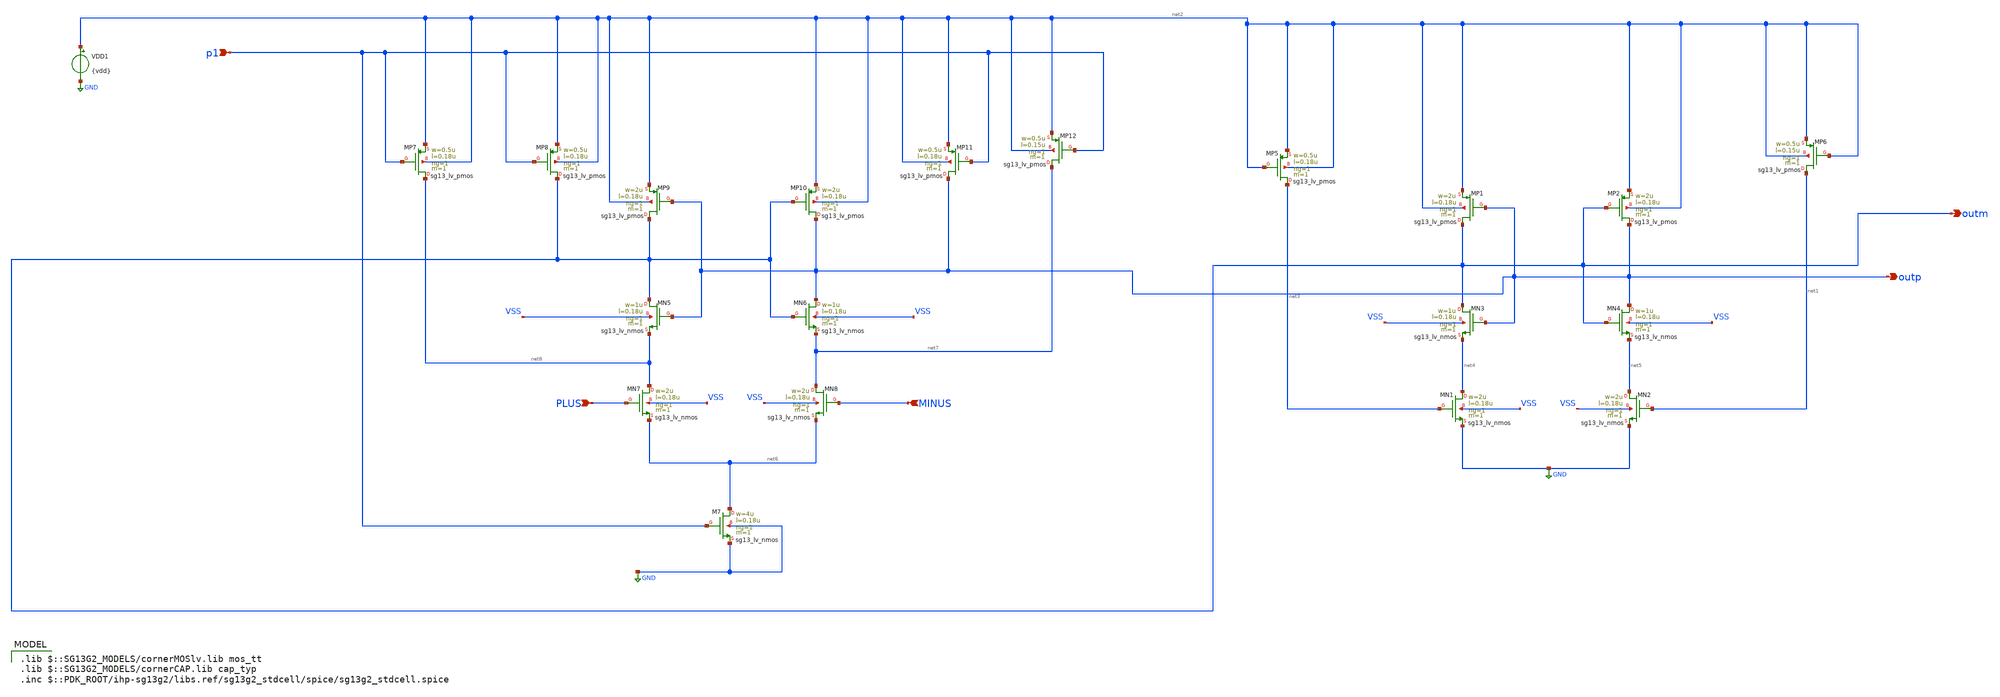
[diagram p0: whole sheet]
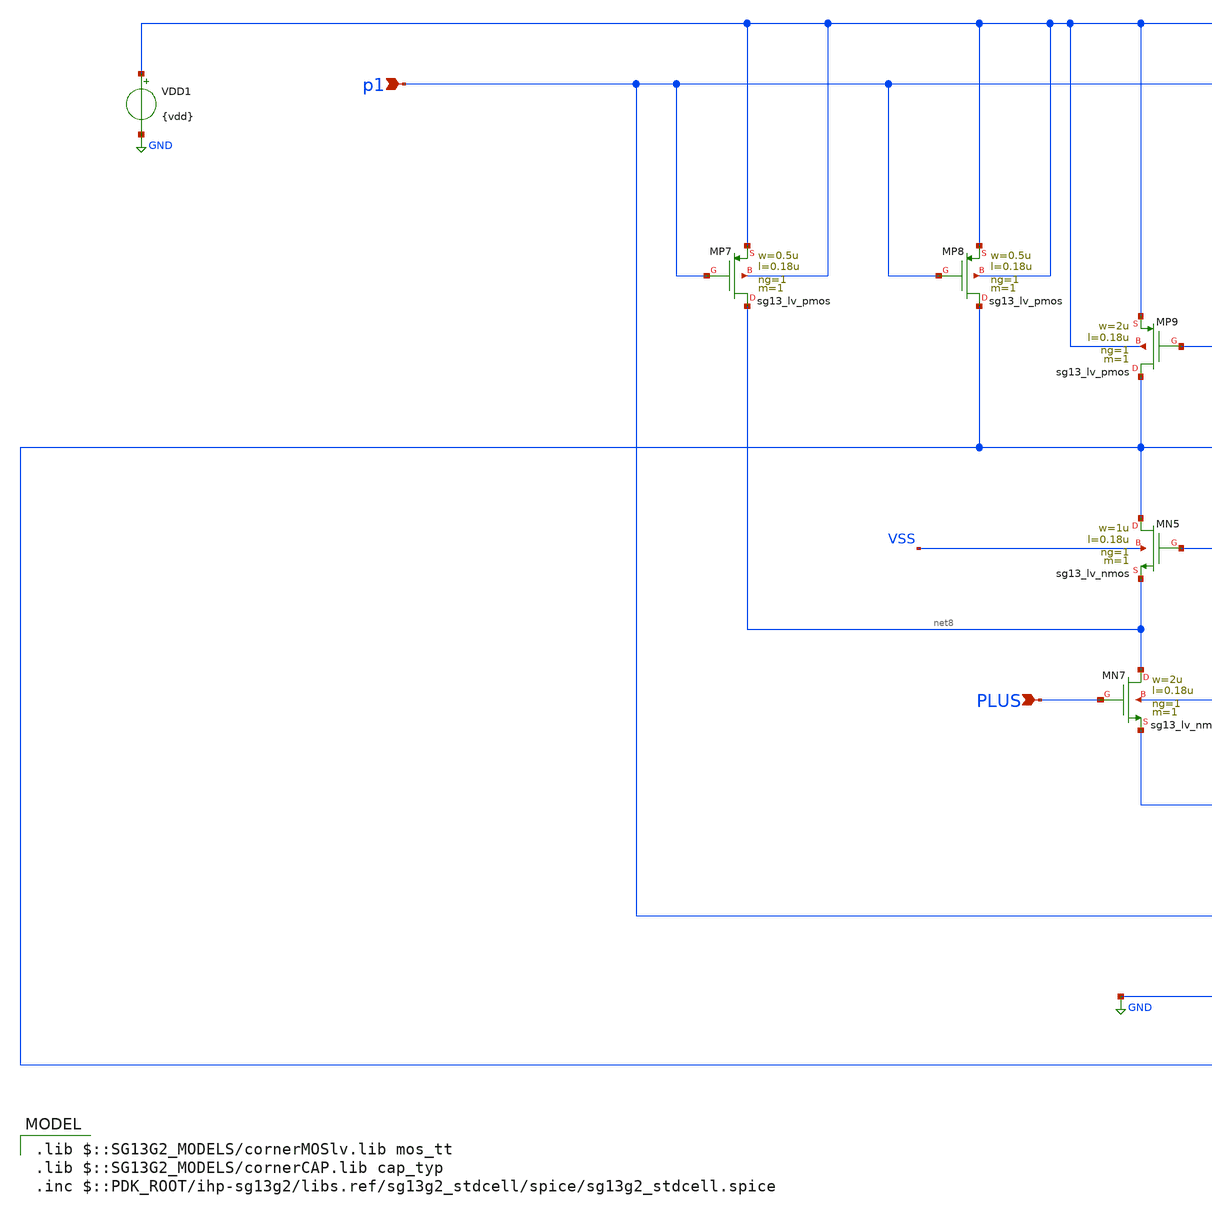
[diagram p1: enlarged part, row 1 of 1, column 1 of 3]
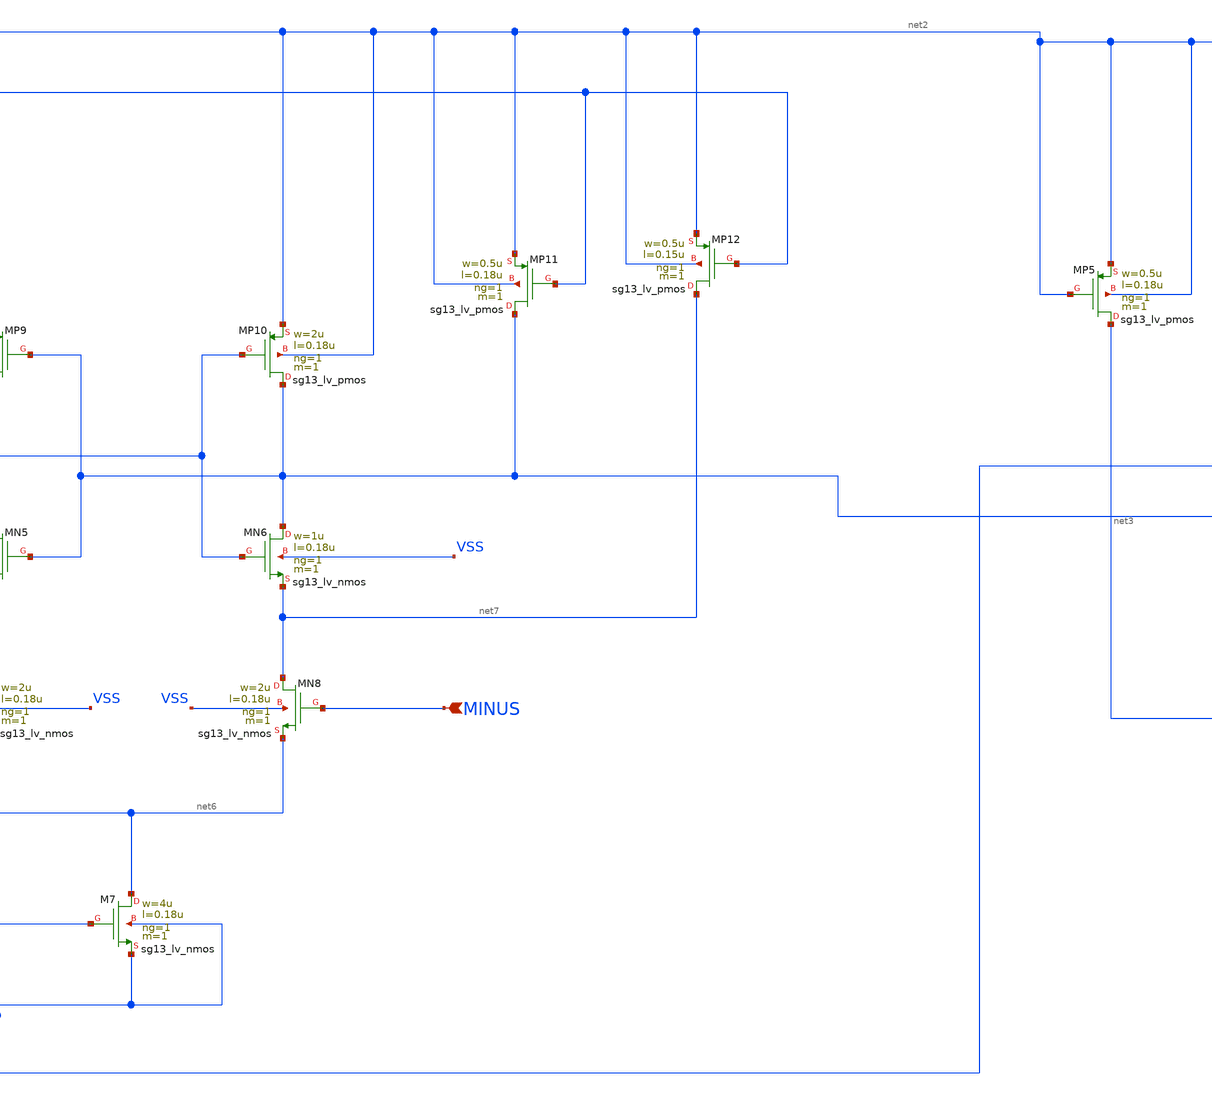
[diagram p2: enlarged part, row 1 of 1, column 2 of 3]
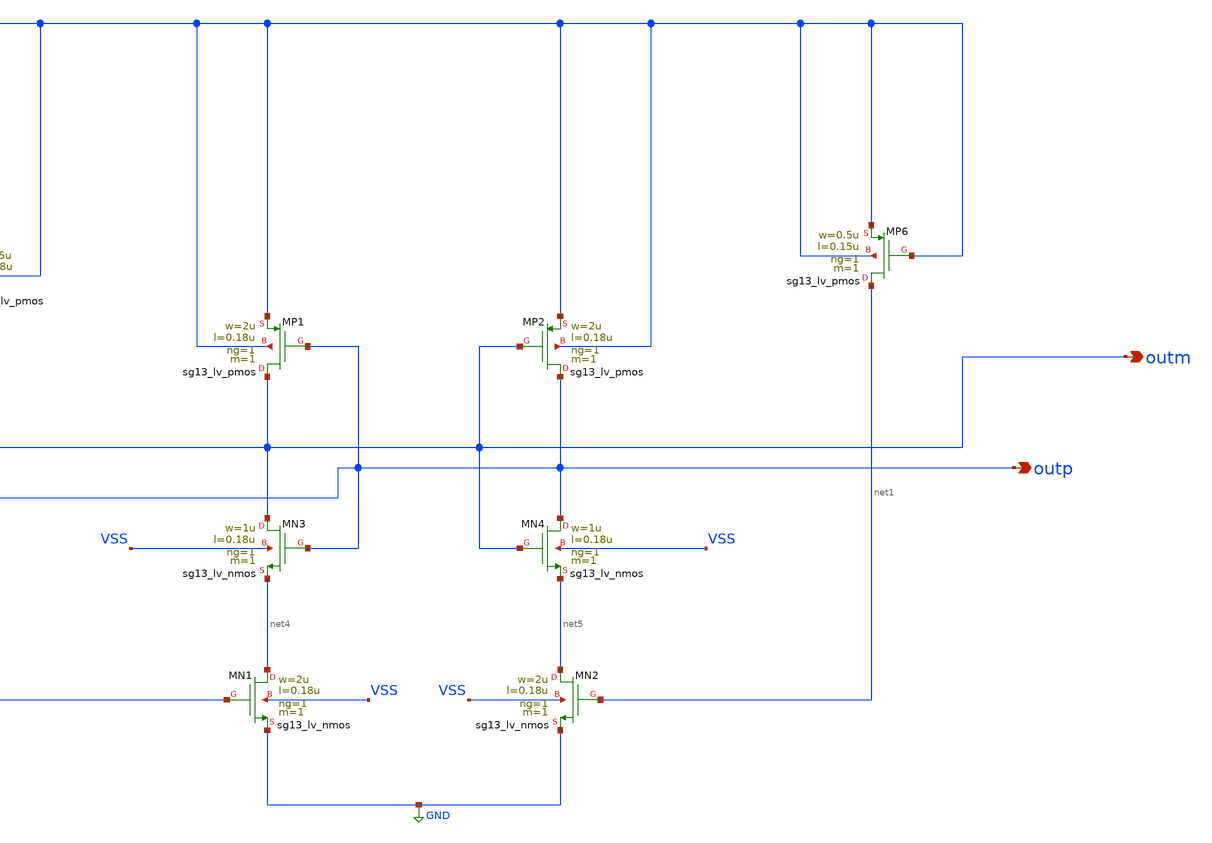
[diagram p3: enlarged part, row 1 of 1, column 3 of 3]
** sch_path: CEMS_G2/DSM/Schematics/RealCircuits/Comp-Latch.sch
**.subckt Comp-Latch outp PLUS MINUS p1 outm
*.opin outp
*.ipin PLUS
*.ipin MINUS
*.ipin p1
*.opin outm
XMN3 outm outp net4 VSS sg13_lv_nmos w=1u l=0.18u ng=1 m=1 mm_ok=1
XMP5 net3 net2 net2 net2 sg13_lv_pmos w=0.5u l=0.18u ng=1 m=1 mm_ok=1
XMP1 outm outp net2 net2 sg13_lv_pmos w=2u l=0.18u ng=1 m=1 mm_ok=1
XMP2 outp outm net2 net2 sg13_lv_pmos w=2u l=0.18u ng=1 m=1 mm_ok=1
XMP6 net1 net2 net2 net2 sg13_lv_pmos w=0.5u l=0.15u ng=1 m=1 mm_ok=1
XMN4 outp outm net5 VSS sg13_lv_nmos w=1u l=0.18u ng=1 m=1 mm_ok=1
XMN1 net4 net3 GND VSS sg13_lv_nmos w=2u l=0.18u ng=1 m=1 mm_ok=1
XMN2 net5 net1 GND VSS sg13_lv_nmos w=2u l=0.18u ng=1 m=1 mm_ok=1
XMN5 outm outp net8 VSS sg13_lv_nmos w=1u l=0.18u ng=1 m=1 mm_ok=1
XMP7 net8 p1 net2 net2 sg13_lv_pmos w=0.5u l=0.18u ng=1 m=1 mm_ok=1
XMP8 outm p1 net2 net2 sg13_lv_pmos w=0.5u l=0.18u ng=1 m=1 mm_ok=1
XMP9 outm outp net2 net2 sg13_lv_pmos w=2u l=0.18u ng=1 m=1 mm_ok=1
XMP10 outp outm net2 net2 sg13_lv_pmos w=2u l=0.18u ng=1 m=1 mm_ok=1
XMP11 outp p1 net2 net2 sg13_lv_pmos w=0.5u l=0.18u ng=1 m=1 mm_ok=1
XMP12 net7 p1 net2 net2 sg13_lv_pmos w=0.5u l=0.15u ng=1 m=1 mm_ok=1
XMN6 outp outm net7 VSS sg13_lv_nmos w=1u l=0.18u ng=1 m=1 mm_ok=1
XMN7 net8 PLUS net6 VSS sg13_lv_nmos w=2u l=0.18u ng=1 m=1 mm_ok=1
XMN8 net7 MINUS net6 VSS sg13_lv_nmos w=2u l=0.18u ng=1 m=1 mm_ok=1
XM7 net6 p1 GND GND sg13_lv_nmos w=4u l=0.18u ng=1 m=1 mm_ok=1
VDD1 net2 GND {vdd}
**** begin user architecture code
 .lib $::SG13G2_MODELS/cornerMOSlv.lib mos_tt
.lib $::SG13G2_MODELS/cornerCAP.lib cap_typ
.inc $::PDK_ROOT/ihp-sg13g2/libs.ref/sg13g2_stdcell/spice/sg13g2_stdcell.spice

**** end user architecture code
**.ends
.GLOBAL GND
.end
